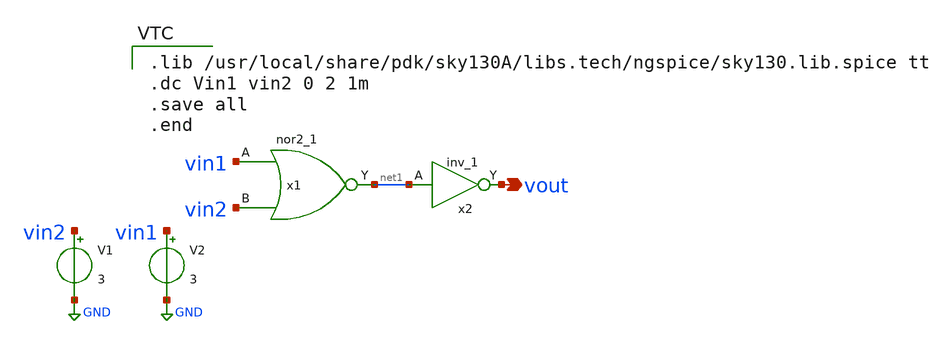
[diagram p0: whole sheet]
** sch_path: orgate.sch
**.subckt orgate vout
*.opin vout
x1 vin1 vin2 VGND VNB VPB VPWR net1 sky130_fd_sc_hd__nor2_1
x2 net1 VGND VNB VPB VPWR vout sky130_fd_sc_hd__inv_1
V1 vin2 GND 3
V2 vin1 GND 3
**** begin user architecture code

.lib /usr/local/share/pdk/sky130A/libs.tech/ngspice/sky130.lib.spice tt
.dc Vin1 vin2 0 2 1m
.save all
.end

**** end user architecture code
**.ends
.GLOBAL GND
.end
